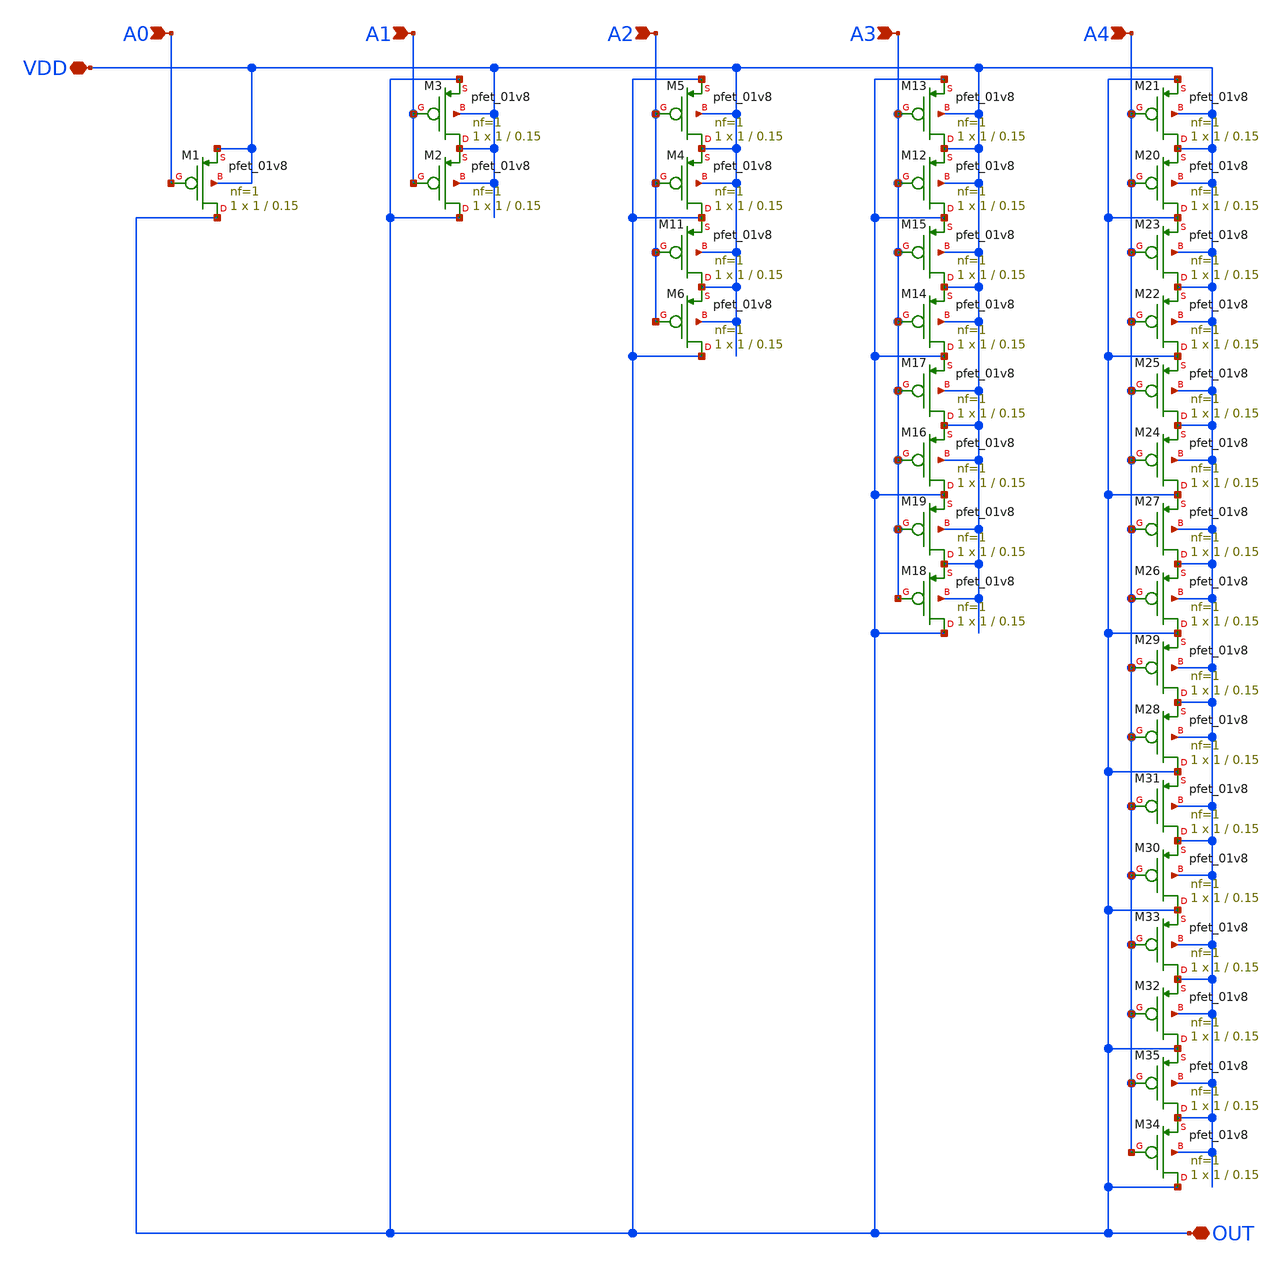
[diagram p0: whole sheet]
** sch_path: libs.ref/sky130_hilas_sc/xschem/sky130_hilas_DAC5bit01.sch
**.subckt sky130_hilas_DAC5bit01 VDD A4 OUT A3 A2 A1 A0
*.iopin VDD
*.ipin A4
*.iopin OUT
*.ipin A3
*.ipin A2
*.ipin A1
*.ipin A0
XM1 OUT A0 VDD VDD sky130_fd_pr__pfet_01v8 L=0.15 W=1 nf=1 ad='int((nf+1)/2) * W/nf * 0.29' as='int((nf+2)/2) * W/nf * 0.29'
+ pd='2*int((nf+1)/2) * (W/nf + 0.29)' ps='2*int((nf+2)/2) * (W/nf + 0.29)' nrd='0.29 / W' nrs='0.29 / W'
+ sa=0 sb=0 sd=0 mult=1 m=1
XM2 OUT A1 VDD VDD sky130_fd_pr__pfet_01v8 L=0.15 W=1 nf=1 ad='int((nf+1)/2) * W/nf * 0.29' as='int((nf+2)/2) * W/nf * 0.29'
+ pd='2*int((nf+1)/2) * (W/nf + 0.29)' ps='2*int((nf+2)/2) * (W/nf + 0.29)' nrd='0.29 / W' nrs='0.29 / W'
+ sa=0 sb=0 sd=0 mult=1 m=1
XM3 VDD A1 OUT VDD sky130_fd_pr__pfet_01v8 L=0.15 W=1 nf=1 ad='int((nf+1)/2) * W/nf * 0.29' as='int((nf+2)/2) * W/nf * 0.29'
+ pd='2*int((nf+1)/2) * (W/nf + 0.29)' ps='2*int((nf+2)/2) * (W/nf + 0.29)' nrd='0.29 / W' nrs='0.29 / W'
+ sa=0 sb=0 sd=0 mult=1 m=1
XM4 OUT A2 VDD VDD sky130_fd_pr__pfet_01v8 L=0.15 W=1 nf=1 ad='int((nf+1)/2) * W/nf * 0.29' as='int((nf+2)/2) * W/nf * 0.29'
+ pd='2*int((nf+1)/2) * (W/nf + 0.29)' ps='2*int((nf+2)/2) * (W/nf + 0.29)' nrd='0.29 / W' nrs='0.29 / W'
+ sa=0 sb=0 sd=0 mult=1 m=1
XM5 VDD A2 OUT VDD sky130_fd_pr__pfet_01v8 L=0.15 W=1 nf=1 ad='int((nf+1)/2) * W/nf * 0.29' as='int((nf+2)/2) * W/nf * 0.29'
+ pd='2*int((nf+1)/2) * (W/nf + 0.29)' ps='2*int((nf+2)/2) * (W/nf + 0.29)' nrd='0.29 / W' nrs='0.29 / W'
+ sa=0 sb=0 sd=0 mult=1 m=1
XM6 OUT A2 VDD VDD sky130_fd_pr__pfet_01v8 L=0.15 W=1 nf=1 ad='int((nf+1)/2) * W/nf * 0.29' as='int((nf+2)/2) * W/nf * 0.29'
+ pd='2*int((nf+1)/2) * (W/nf + 0.29)' ps='2*int((nf+2)/2) * (W/nf + 0.29)' nrd='0.29 / W' nrs='0.29 / W'
+ sa=0 sb=0 sd=0 mult=1 m=1
XM11 VDD A2 OUT VDD sky130_fd_pr__pfet_01v8 L=0.15 W=1 nf=1 ad='int((nf+1)/2) * W/nf * 0.29' as='int((nf+2)/2) * W/nf * 0.29'
+ pd='2*int((nf+1)/2) * (W/nf + 0.29)' ps='2*int((nf+2)/2) * (W/nf + 0.29)' nrd='0.29 / W' nrs='0.29 / W'
+ sa=0 sb=0 sd=0 mult=1 m=1
XM12 OUT A3 VDD VDD sky130_fd_pr__pfet_01v8 L=0.15 W=1 nf=1 ad='int((nf+1)/2) * W/nf * 0.29' as='int((nf+2)/2) * W/nf * 0.29'
+ pd='2*int((nf+1)/2) * (W/nf + 0.29)' ps='2*int((nf+2)/2) * (W/nf + 0.29)' nrd='0.29 / W' nrs='0.29 / W'
+ sa=0 sb=0 sd=0 mult=1 m=1
XM13 VDD A3 OUT VDD sky130_fd_pr__pfet_01v8 L=0.15 W=1 nf=1 ad='int((nf+1)/2) * W/nf * 0.29' as='int((nf+2)/2) * W/nf * 0.29'
+ pd='2*int((nf+1)/2) * (W/nf + 0.29)' ps='2*int((nf+2)/2) * (W/nf + 0.29)' nrd='0.29 / W' nrs='0.29 / W'
+ sa=0 sb=0 sd=0 mult=1 m=1
XM14 OUT A3 VDD VDD sky130_fd_pr__pfet_01v8 L=0.15 W=1 nf=1 ad='int((nf+1)/2) * W/nf * 0.29' as='int((nf+2)/2) * W/nf * 0.29'
+ pd='2*int((nf+1)/2) * (W/nf + 0.29)' ps='2*int((nf+2)/2) * (W/nf + 0.29)' nrd='0.29 / W' nrs='0.29 / W'
+ sa=0 sb=0 sd=0 mult=1 m=1
XM15 VDD A3 OUT VDD sky130_fd_pr__pfet_01v8 L=0.15 W=1 nf=1 ad='int((nf+1)/2) * W/nf * 0.29' as='int((nf+2)/2) * W/nf * 0.29'
+ pd='2*int((nf+1)/2) * (W/nf + 0.29)' ps='2*int((nf+2)/2) * (W/nf + 0.29)' nrd='0.29 / W' nrs='0.29 / W'
+ sa=0 sb=0 sd=0 mult=1 m=1
XM16 OUT A3 VDD VDD sky130_fd_pr__pfet_01v8 L=0.15 W=1 nf=1 ad='int((nf+1)/2) * W/nf * 0.29' as='int((nf+2)/2) * W/nf * 0.29'
+ pd='2*int((nf+1)/2) * (W/nf + 0.29)' ps='2*int((nf+2)/2) * (W/nf + 0.29)' nrd='0.29 / W' nrs='0.29 / W'
+ sa=0 sb=0 sd=0 mult=1 m=1
XM17 VDD A3 OUT VDD sky130_fd_pr__pfet_01v8 L=0.15 W=1 nf=1 ad='int((nf+1)/2) * W/nf * 0.29' as='int((nf+2)/2) * W/nf * 0.29'
+ pd='2*int((nf+1)/2) * (W/nf + 0.29)' ps='2*int((nf+2)/2) * (W/nf + 0.29)' nrd='0.29 / W' nrs='0.29 / W'
+ sa=0 sb=0 sd=0 mult=1 m=1
XM18 OUT A3 VDD VDD sky130_fd_pr__pfet_01v8 L=0.15 W=1 nf=1 ad='int((nf+1)/2) * W/nf * 0.29' as='int((nf+2)/2) * W/nf * 0.29'
+ pd='2*int((nf+1)/2) * (W/nf + 0.29)' ps='2*int((nf+2)/2) * (W/nf + 0.29)' nrd='0.29 / W' nrs='0.29 / W'
+ sa=0 sb=0 sd=0 mult=1 m=1
XM19 VDD A3 OUT VDD sky130_fd_pr__pfet_01v8 L=0.15 W=1 nf=1 ad='int((nf+1)/2) * W/nf * 0.29' as='int((nf+2)/2) * W/nf * 0.29'
+ pd='2*int((nf+1)/2) * (W/nf + 0.29)' ps='2*int((nf+2)/2) * (W/nf + 0.29)' nrd='0.29 / W' nrs='0.29 / W'
+ sa=0 sb=0 sd=0 mult=1 m=1
XM20 OUT A4 VDD VDD sky130_fd_pr__pfet_01v8 L=0.15 W=1 nf=1 ad='int((nf+1)/2) * W/nf * 0.29' as='int((nf+2)/2) * W/nf * 0.29'
+ pd='2*int((nf+1)/2) * (W/nf + 0.29)' ps='2*int((nf+2)/2) * (W/nf + 0.29)' nrd='0.29 / W' nrs='0.29 / W'
+ sa=0 sb=0 sd=0 mult=1 m=1
XM21 VDD A4 OUT VDD sky130_fd_pr__pfet_01v8 L=0.15 W=1 nf=1 ad='int((nf+1)/2) * W/nf * 0.29' as='int((nf+2)/2) * W/nf * 0.29'
+ pd='2*int((nf+1)/2) * (W/nf + 0.29)' ps='2*int((nf+2)/2) * (W/nf + 0.29)' nrd='0.29 / W' nrs='0.29 / W'
+ sa=0 sb=0 sd=0 mult=1 m=1
XM22 OUT A4 VDD VDD sky130_fd_pr__pfet_01v8 L=0.15 W=1 nf=1 ad='int((nf+1)/2) * W/nf * 0.29' as='int((nf+2)/2) * W/nf * 0.29'
+ pd='2*int((nf+1)/2) * (W/nf + 0.29)' ps='2*int((nf+2)/2) * (W/nf + 0.29)' nrd='0.29 / W' nrs='0.29 / W'
+ sa=0 sb=0 sd=0 mult=1 m=1
XM23 VDD A4 OUT VDD sky130_fd_pr__pfet_01v8 L=0.15 W=1 nf=1 ad='int((nf+1)/2) * W/nf * 0.29' as='int((nf+2)/2) * W/nf * 0.29'
+ pd='2*int((nf+1)/2) * (W/nf + 0.29)' ps='2*int((nf+2)/2) * (W/nf + 0.29)' nrd='0.29 / W' nrs='0.29 / W'
+ sa=0 sb=0 sd=0 mult=1 m=1
XM24 OUT A4 VDD VDD sky130_fd_pr__pfet_01v8 L=0.15 W=1 nf=1 ad='int((nf+1)/2) * W/nf * 0.29' as='int((nf+2)/2) * W/nf * 0.29'
+ pd='2*int((nf+1)/2) * (W/nf + 0.29)' ps='2*int((nf+2)/2) * (W/nf + 0.29)' nrd='0.29 / W' nrs='0.29 / W'
+ sa=0 sb=0 sd=0 mult=1 m=1
XM25 VDD A4 OUT VDD sky130_fd_pr__pfet_01v8 L=0.15 W=1 nf=1 ad='int((nf+1)/2) * W/nf * 0.29' as='int((nf+2)/2) * W/nf * 0.29'
+ pd='2*int((nf+1)/2) * (W/nf + 0.29)' ps='2*int((nf+2)/2) * (W/nf + 0.29)' nrd='0.29 / W' nrs='0.29 / W'
+ sa=0 sb=0 sd=0 mult=1 m=1
XM26 OUT A4 VDD VDD sky130_fd_pr__pfet_01v8 L=0.15 W=1 nf=1 ad='int((nf+1)/2) * W/nf * 0.29' as='int((nf+2)/2) * W/nf * 0.29'
+ pd='2*int((nf+1)/2) * (W/nf + 0.29)' ps='2*int((nf+2)/2) * (W/nf + 0.29)' nrd='0.29 / W' nrs='0.29 / W'
+ sa=0 sb=0 sd=0 mult=1 m=1
XM27 VDD A4 OUT VDD sky130_fd_pr__pfet_01v8 L=0.15 W=1 nf=1 ad='int((nf+1)/2) * W/nf * 0.29' as='int((nf+2)/2) * W/nf * 0.29'
+ pd='2*int((nf+1)/2) * (W/nf + 0.29)' ps='2*int((nf+2)/2) * (W/nf + 0.29)' nrd='0.29 / W' nrs='0.29 / W'
+ sa=0 sb=0 sd=0 mult=1 m=1
XM28 OUT A4 VDD VDD sky130_fd_pr__pfet_01v8 L=0.15 W=1 nf=1 ad='int((nf+1)/2) * W/nf * 0.29' as='int((nf+2)/2) * W/nf * 0.29'
+ pd='2*int((nf+1)/2) * (W/nf + 0.29)' ps='2*int((nf+2)/2) * (W/nf + 0.29)' nrd='0.29 / W' nrs='0.29 / W'
+ sa=0 sb=0 sd=0 mult=1 m=1
XM29 VDD A4 OUT VDD sky130_fd_pr__pfet_01v8 L=0.15 W=1 nf=1 ad='int((nf+1)/2) * W/nf * 0.29' as='int((nf+2)/2) * W/nf * 0.29'
+ pd='2*int((nf+1)/2) * (W/nf + 0.29)' ps='2*int((nf+2)/2) * (W/nf + 0.29)' nrd='0.29 / W' nrs='0.29 / W'
+ sa=0 sb=0 sd=0 mult=1 m=1
XM30 OUT A4 VDD VDD sky130_fd_pr__pfet_01v8 L=0.15 W=1 nf=1 ad='int((nf+1)/2) * W/nf * 0.29' as='int((nf+2)/2) * W/nf * 0.29'
+ pd='2*int((nf+1)/2) * (W/nf + 0.29)' ps='2*int((nf+2)/2) * (W/nf + 0.29)' nrd='0.29 / W' nrs='0.29 / W'
+ sa=0 sb=0 sd=0 mult=1 m=1
XM31 VDD A4 OUT VDD sky130_fd_pr__pfet_01v8 L=0.15 W=1 nf=1 ad='int((nf+1)/2) * W/nf * 0.29' as='int((nf+2)/2) * W/nf * 0.29'
+ pd='2*int((nf+1)/2) * (W/nf + 0.29)' ps='2*int((nf+2)/2) * (W/nf + 0.29)' nrd='0.29 / W' nrs='0.29 / W'
+ sa=0 sb=0 sd=0 mult=1 m=1
XM32 OUT A4 VDD VDD sky130_fd_pr__pfet_01v8 L=0.15 W=1 nf=1 ad='int((nf+1)/2) * W/nf * 0.29' as='int((nf+2)/2) * W/nf * 0.29'
+ pd='2*int((nf+1)/2) * (W/nf + 0.29)' ps='2*int((nf+2)/2) * (W/nf + 0.29)' nrd='0.29 / W' nrs='0.29 / W'
+ sa=0 sb=0 sd=0 mult=1 m=1
XM33 VDD A4 OUT VDD sky130_fd_pr__pfet_01v8 L=0.15 W=1 nf=1 ad='int((nf+1)/2) * W/nf * 0.29' as='int((nf+2)/2) * W/nf * 0.29'
+ pd='2*int((nf+1)/2) * (W/nf + 0.29)' ps='2*int((nf+2)/2) * (W/nf + 0.29)' nrd='0.29 / W' nrs='0.29 / W'
+ sa=0 sb=0 sd=0 mult=1 m=1
XM34 OUT A4 VDD VDD sky130_fd_pr__pfet_01v8 L=0.15 W=1 nf=1 ad='int((nf+1)/2) * W/nf * 0.29' as='int((nf+2)/2) * W/nf * 0.29'
+ pd='2*int((nf+1)/2) * (W/nf + 0.29)' ps='2*int((nf+2)/2) * (W/nf + 0.29)' nrd='0.29 / W' nrs='0.29 / W'
+ sa=0 sb=0 sd=0 mult=1 m=1
XM35 VDD A4 OUT VDD sky130_fd_pr__pfet_01v8 L=0.15 W=1 nf=1 ad='int((nf+1)/2) * W/nf * 0.29' as='int((nf+2)/2) * W/nf * 0.29'
+ pd='2*int((nf+1)/2) * (W/nf + 0.29)' ps='2*int((nf+2)/2) * (W/nf + 0.29)' nrd='0.29 / W' nrs='0.29 / W'
+ sa=0 sb=0 sd=0 mult=1 m=1
**.ends
.end
